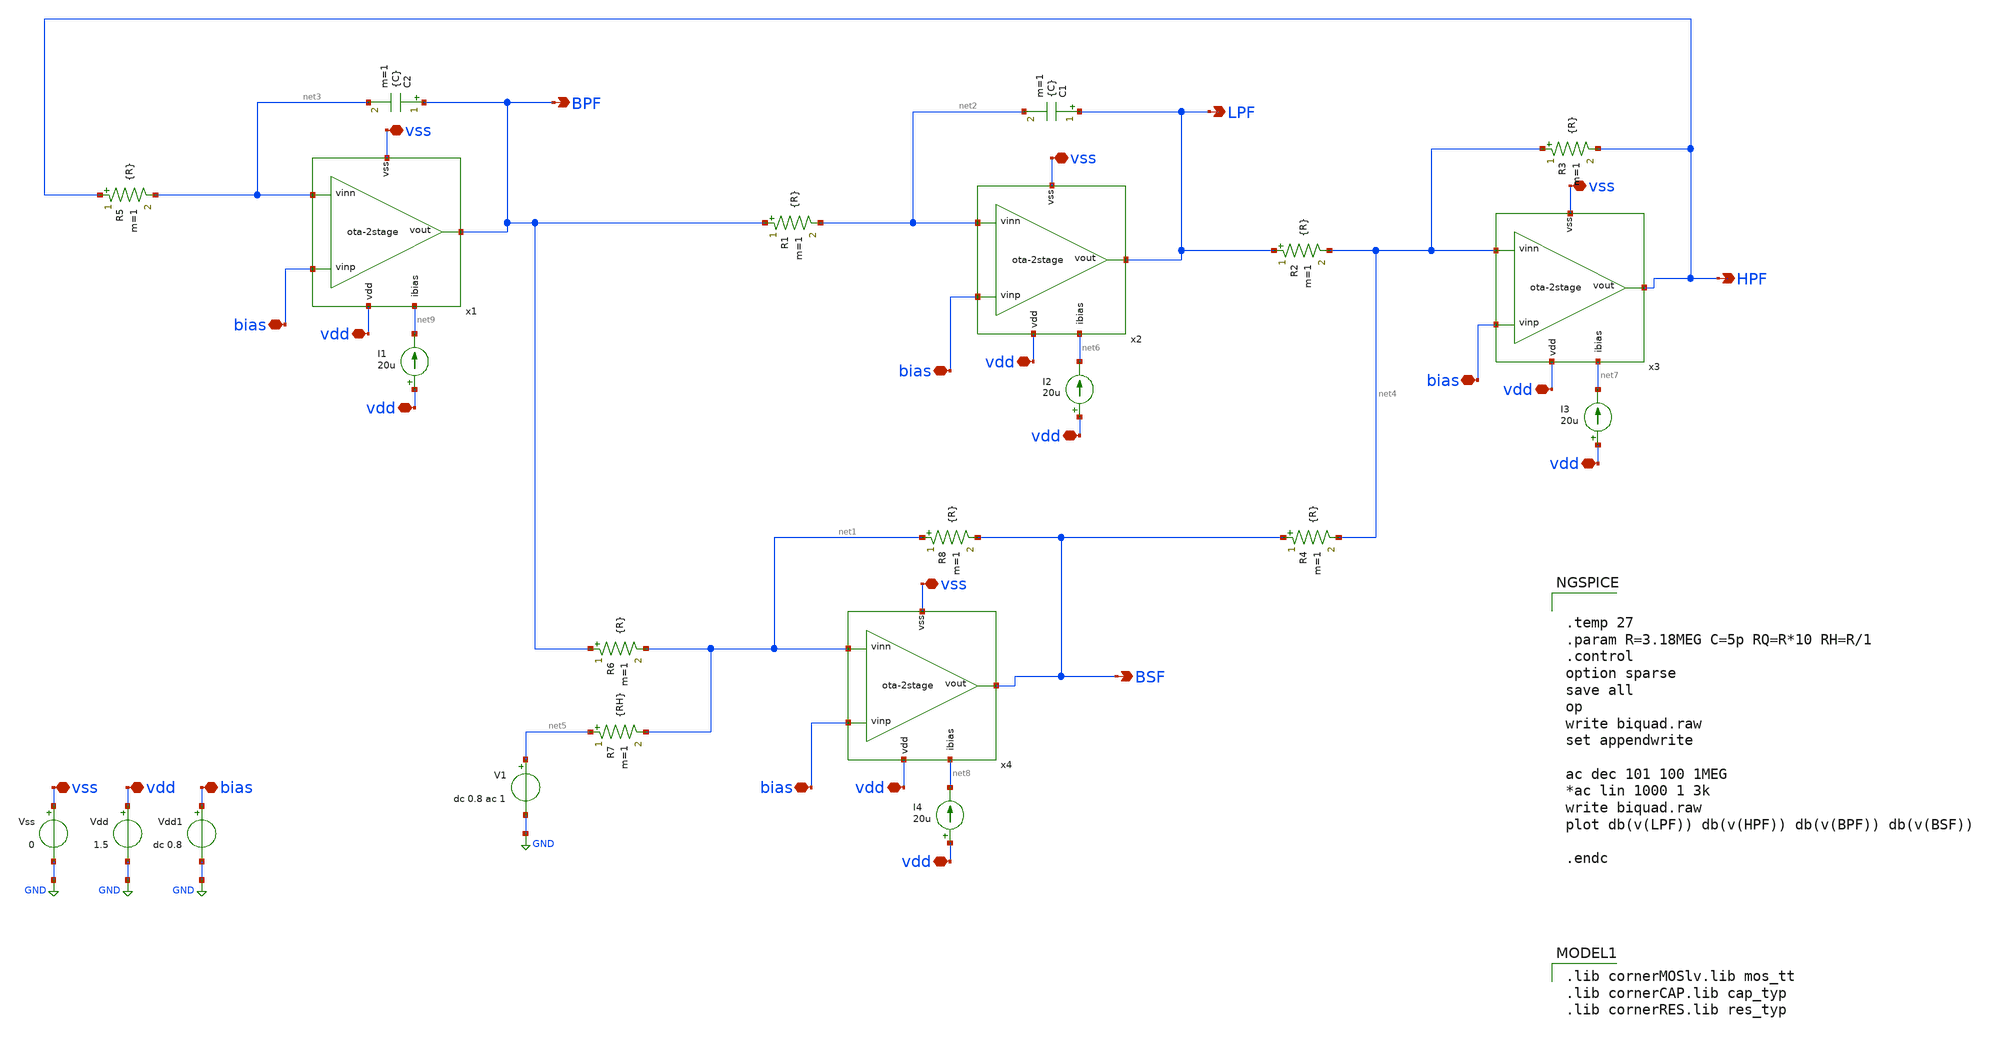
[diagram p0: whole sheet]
** sch_path: Testbench/2stage-ota_tb-biquad_univ.sch
**.subckt 2stage-ota_tb-biquad_univ HPF BSF LPF BPF vss vdd vdd vss vdd vss vss vdd vdd bias bias
*+ bias bias bias vss vdd vdd vdd vdd
*.opin HPF
*.opin BSF
*.opin LPF
*.opin BPF
*.iopin vss
*.iopin vdd
*.iopin vdd
*.iopin vss
*.iopin vdd
*.iopin vss
*.iopin vss
*.iopin vdd
*.iopin vdd
*.iopin bias
*.iopin bias
*.iopin bias
*.iopin bias
*.iopin bias
*.iopin vss
*.iopin vdd
*.iopin vdd
*.iopin vdd
*.iopin vdd
C1 LPF net2 {C} m=1
C2 BPF net3 {C} m=1
R1 BPF net2 {R} m=1
R2 LPF net4 {R} m=1
R3 net4 HPF {R} m=1
R4 BSF net4 {R} m=1
R5 HPF net3 {R} m=1
R6 BPF net1 {R} m=1
R7 net5 net1 {RH} m=1
R8 net1 BSF {R} m=1
V1 net5 GND dc 0.8 ac 1
x1 vdd net9 net3 BPF bias vss ota-2stage
Vdd vdd GND 1.5
Vss vss GND 0
x2 vdd net6 net2 LPF bias vss ota-2stage
x3 vdd net7 net4 HPF bias vss ota-2stage
x4 vdd net8 net1 BSF bias vss ota-2stage
Vdd1 bias GND dc 0.8
I1 vdd net9 20u
I2 vdd net6 20u
I3 vdd net7 20u
I4 vdd net8 20u
**** begin user architecture code


.temp 27
.param R=3.18MEG C=5p RQ=R*10 RH=R/1
.control
option sparse
save all
op
write biquad.raw
set appendwrite

ac dec 101 100 1MEG
*ac lin 1000 1 3k
write biquad.raw
plot db(v(LPF)) db(v(HPF)) db(v(BPF)) db(v(BSF))

.endc


 .lib cornerMOSlv.lib mos_tt
.lib cornerCAP.lib cap_typ
.lib cornerRES.lib res_typ

**** end user architecture code
**.ends

* expanding   symbol:  ota-2stage.sym # of pins=6
** sym_path: Testbench/ota-2stage.sym
** sch_path: Testbench/ota-2stage.sch
.subckt ota-2stage vdd ibias vinn vout vinp vss
*.iopin vdd
*.iopin vss
*.ipin ibias
*.iopin vout
*.ipin vinn
*.ipin vinp
XM1 net1 vinn net3 net3 sg13_lv_nmos w=1u l=2u ng=1 m=1 mm_ok=1
XM2 net2 vinp net3 net3 sg13_lv_nmos w=1u l=2u ng=1 m=1 mm_ok=1
XM4 net2 net1 vdd vdd sg13_lv_pmos w=1u l=2u ng=1 m=1 mm_ok=1
XM3 net1 net1 vdd vdd sg13_lv_pmos w=1u l=2u ng=1 m=1 mm_ok=1
XM5 vout net2 vdd vdd sg13_lv_pmos w=9.5u l=2u ng=1 m=1 mm_ok=1
XM6 ibias ibias vss vss sg13_lv_nmos w=2u l=2u ng=1 m=1 mm_ok=1
XM7 net3 ibias vss vss sg13_lv_nmos w=0.5u l=2u ng=1 m=1 mm_ok=1
XM8 vout ibias vss vss sg13_lv_nmos w=1u l=2u ng=1 m=1 mm_ok=1
XCM vout net4 cap_cmim w=19.5e-6 l=19.5e-6 m=1 mm_ok=1
XRN net2 net4 GND rhigh w=1e-6 l=12.6e-6 m=1 b=0 mm_ok=1
.ends

.GLOBAL GND
.end
